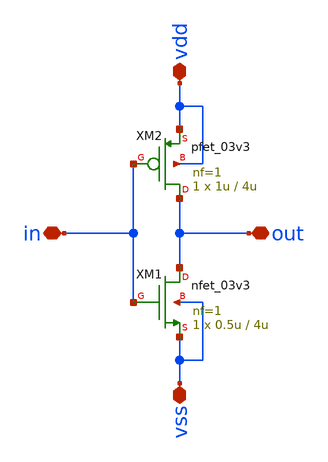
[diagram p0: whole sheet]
** sch_path: designs/libs/qw_core_analog/SmallW_Linv_2/SmallW_Linv_2.sch
**.subckt SmallW_Linv_2 in out vdd vss
*.iopin in
*.iopin out
*.iopin vdd
*.iopin vss
XM1 out in vss vss nfet_03v3 L=4u W=0.5u nf=1 ad='int((nf+1)/2) * W/nf * 0.18u' as='int((nf+2)/2) * W/nf * 0.18u'
+ pd='2*int((nf+1)/2) * (W/nf + 0.18u)' ps='2*int((nf+2)/2) * (W/nf + 0.18u)' nrd='0.18u / W' nrs='0.18u / W'
+ sa=0 sb=0 sd=0 m=1
XM2 out in vdd vdd pfet_03v3 L=4u W=1u nf=1 ad='int((nf+1)/2) * W/nf * 0.18u' as='int((nf+2)/2) * W/nf * 0.18u'
+ pd='2*int((nf+1)/2) * (W/nf + 0.18u)' ps='2*int((nf+2)/2) * (W/nf + 0.18u)' nrd='0.18u / W' nrs='0.18u / W'
+ sa=0 sb=0 sd=0 m=1
**.ends
.end
